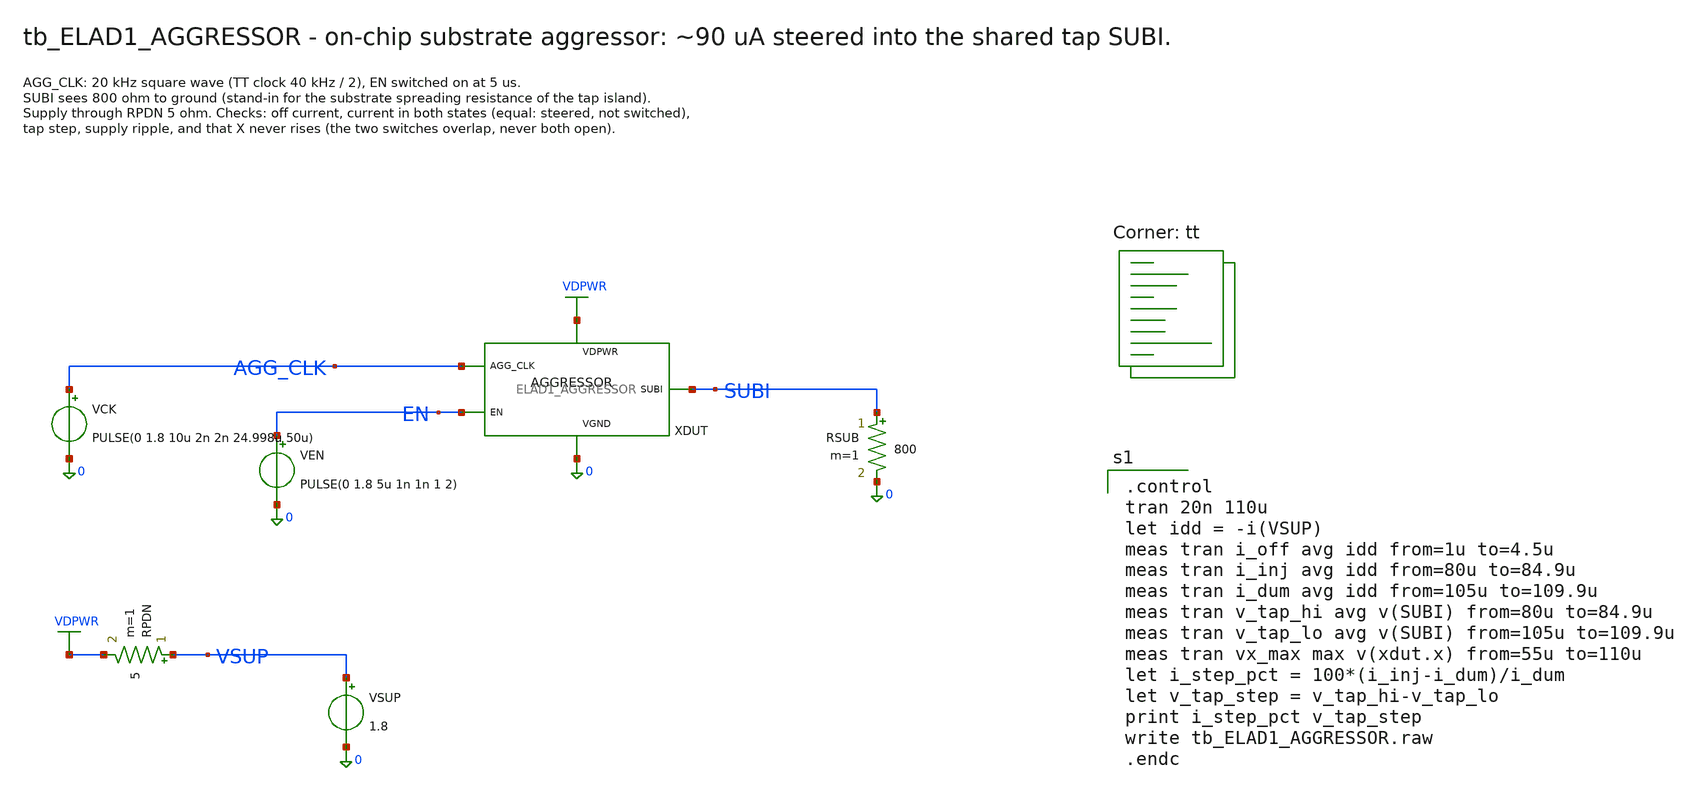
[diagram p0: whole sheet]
** sch_path: cells/ELAD1_AGGRESSOR/schematic/tb_ELAD1_AGGRESSOR.sch
**.subckt tb_ELAD1_AGGRESSOR
XDUT AGG_CLK EN VDPWR 0 SUBI ELAD1_AGGRESSOR
VEN EN 0 PULSE(0 1.8 5u 1n 1n 1 2)
VCK AGG_CLK 0 PULSE(0 1.8 10u 2n 2n 24.998u 50u)
RSUB SUBI 0 800 m=1
RPDN VSUP VDPWR 5 m=1
VSUP VSUP 0 1.8
**** begin user architecture code

.control
tran 20n 110u
let idd = -i(VSUP)
meas tran i_off avg idd from=1u to=4.5u
meas tran i_inj avg idd from=80u to=84.9u
meas tran i_dum avg idd from=105u to=109.9u
meas tran v_tap_hi avg v(SUBI) from=80u to=84.9u
meas tran v_tap_lo avg v(SUBI) from=105u to=109.9u
meas tran vx_max max v(xdut.x) from=55u to=110u
let i_step_pct = 100*(i_inj-i_dum)/i_dum
let v_tap_step = v_tap_hi-v_tap_lo
print i_step_pct v_tap_step
write tb_ELAD1_AGGRESSOR.raw
.endc

.lib $::SKYWATER_MODELS/sky130.lib.spice tt
**** end user architecture code
**.ends

* expanding   symbol:  ELAD1_AGGRESSOR.sym # of pins=5
** sym_path: cells/ELAD1_AGGRESSOR/schematic/ELAD1_AGGRESSOR.sym
** sch_path: cells/ELAD1_AGGRESSOR/schematic/ELAD1_AGGRESSOR.sch
.subckt ELAD1_AGGRESSOR AGG_CLK EN VDPWR VGND SUBI
*.iopin AGG_CLK
*.iopin EN
*.iopin VDPWR
*.iopin VGND
*.iopin SUBI
XIC AGG_CLK CKB VDPWR VGND ELAD1_INV
XIE EN ENB VDPWR VGND ELAD1_INV
XGIP1 gip ENB VDPWR VDPWR sky130_fd_pr__pfet_01v8 L=0.15 W=2 nf=1 ad='int((nf+1)/2) * W/nf * 0.29' as='int((nf+2)/2) * W/nf * 0.29'
+ pd='2*int((nf+1)/2) * (W/nf + 0.29)' ps='2*int((nf+2)/2) * (W/nf + 0.29)' nrd='0.29 / W' nrs='0.29 / W'
+ sa=0 sb=0 sd=0 mult=1 m=1
XGIP2 GI CKB gip VDPWR sky130_fd_pr__pfet_01v8 L=0.15 W=2 nf=1 ad='int((nf+1)/2) * W/nf * 0.29' as='int((nf+2)/2) * W/nf * 0.29'
+ pd='2*int((nf+1)/2) * (W/nf + 0.29)' ps='2*int((nf+2)/2) * (W/nf + 0.29)' nrd='0.29 / W' nrs='0.29 / W'
+ sa=0 sb=0 sd=0 mult=1 m=1
XGIN1 GI ENB VGND VGND sky130_fd_pr__nfet_01v8 L=1 W=0.42 nf=1 ad='int((1 + 1)/2) * 0.42 / 1 * 0.29'
+ as='int((1 + 2)/2) * 0.42 / 1 * 0.29' pd='2*int((1 + 1)/2) * (0.42 / 1 + 0.29)' ps='2*int((1 + 2)/2) * (0.42 / 1 + 0.29)'
+ nrd='0.29 / 0.42 ' nrs='0.29 / 0.42 ' sa=0 sb=0 sd=0 mult=1 m=1
XGIN2 GI CKB VGND VGND sky130_fd_pr__nfet_01v8 L=1 W=0.42 nf=1 ad='int((1 + 1)/2) * 0.42 / 1 * 0.29'
+ as='int((1 + 2)/2) * 0.42 / 1 * 0.29' pd='2*int((1 + 1)/2) * (0.42 / 1 + 0.29)' ps='2*int((1 + 2)/2) * (0.42 / 1 + 0.29)'
+ nrd='0.29 / 0.42 ' nrs='0.29 / 0.42 ' sa=0 sb=0 sd=0 mult=1 m=1
XGDP1 gdp ENB VDPWR VDPWR sky130_fd_pr__pfet_01v8 L=0.15 W=2 nf=1 ad='int((nf+1)/2) * W/nf * 0.29' as='int((nf+2)/2) * W/nf * 0.29'
+ pd='2*int((nf+1)/2) * (W/nf + 0.29)' ps='2*int((nf+2)/2) * (W/nf + 0.29)' nrd='0.29 / W' nrs='0.29 / W'
+ sa=0 sb=0 sd=0 mult=1 m=1
XGDP2 GD AGG_CLK gdp VDPWR sky130_fd_pr__pfet_01v8 L=0.15 W=2 nf=1 ad='int((nf+1)/2) * W/nf * 0.29' as='int((nf+2)/2) * W/nf * 0.29'
+ pd='2*int((nf+1)/2) * (W/nf + 0.29)' ps='2*int((nf+2)/2) * (W/nf + 0.29)' nrd='0.29 / W' nrs='0.29 / W'
+ sa=0 sb=0 sd=0 mult=1 m=1
XGDN1 GD ENB VGND VGND sky130_fd_pr__nfet_01v8 L=1 W=0.42 nf=1 ad='int((1 + 1)/2) * 0.42 / 1 * 0.29'
+ as='int((1 + 2)/2) * 0.42 / 1 * 0.29' pd='2*int((1 + 1)/2) * (0.42 / 1 + 0.29)' ps='2*int((1 + 2)/2) * (0.42 / 1 + 0.29)'
+ nrd='0.29 / 0.42 ' nrs='0.29 / 0.42 ' sa=0 sb=0 sd=0 mult=1 m=1
XGDN2 GD AGG_CLK VGND VGND sky130_fd_pr__nfet_01v8 L=1 W=0.42 nf=1 ad='int((1 + 1)/2) * 0.42 / 1 * 0.29'
+ as='int((1 + 2)/2) * 0.42 / 1 * 0.29' pd='2*int((1 + 1)/2) * (0.42 / 1 + 0.29)' ps='2*int((1 + 2)/2) * (0.42 / 1 + 0.29)'
+ nrd='0.29 / 0.42 ' nrs='0.29 / 0.42 ' sa=0 sb=0 sd=0 mult=1 m=1
XRL X VDPWR VGND sky130_fd_pr__res_xhigh_po W=0.69 L=7.3 mult=1 m=1
XMINJ X GI SUBI VGND sky130_fd_pr__nfet_01v8 L=0.15 W=2 nf=1 ad='int((1 + 1)/2) * 2 / 1 * 0.29' as='int((1 + 2)/2) * 2 / 1 * 0.29'
+ pd='2*int((1 + 1)/2) * (2 / 1 + 0.29)' ps='2*int((1 + 2)/2) * (2 / 1 + 0.29)' nrd='0.29 / 2 ' nrs='0.29 / 2 '
+ sa=0 sb=0 sd=0 mult=1 m=1
XMDUM X GD D VGND sky130_fd_pr__nfet_01v8 L=0.15 W=2 nf=1 ad='int((1 + 1)/2) * 2 / 1 * 0.29' as='int((1 + 2)/2) * 2 / 1 * 0.29'
+ pd='2*int((1 + 1)/2) * (2 / 1 + 0.29)' ps='2*int((1 + 2)/2) * (2 / 1 + 0.29)' nrd='0.29 / 2 ' nrs='0.29 / 2 '
+ sa=0 sb=0 sd=0 mult=1 m=1
XRDUM VGND D sky130_fd_pr__res_generic_po W=1 L=15 m=1
.ends


* expanding   symbol:  ELAD1_INV.sym # of pins=4
** sym_path: cells/ELAD1_INV/schematic/ELAD1_INV.sym
** sch_path: cells/ELAD1_INV/schematic/ELAD1_INV.sch
.subckt ELAD1_INV A Y VDPWR VGND
*.iopin A
*.iopin Y
*.iopin VDPWR
*.iopin VGND
XMN Y A VGND VGND sky130_fd_pr__nfet_01v8 L=0.15 W=0.65 nf=1 ad='int((1 + 1)/2) * 0.65 / 1 * 0.29' as='int((1 + 2)/2) * 0.65 / 1 * 0.29'
+ pd='2*int((1 + 1)/2) * (0.65 / 1 + 0.29)' ps='2*int((1 + 2)/2) * (0.65 / 1 + 0.29)' nrd='0.29 / 0.65 '
+ nrs='0.29 / 0.65 ' sa=0 sb=0 sd=0 mult=1 m=1
XMP Y A VDPWR VDPWR sky130_fd_pr__pfet_01v8 L=0.15 W=1 nf=1 ad='int((nf+1)/2) * W/nf * 0.29' as='int((nf+2)/2) * W/nf * 0.29'
+ pd='2*int((nf+1)/2) * (W/nf + 0.29)' ps='2*int((nf+2)/2) * (W/nf + 0.29)' nrd='0.29 / W' nrs='0.29 / W'
+ sa=0 sb=0 sd=0 mult=1 m=1
.ends

.GLOBAL VGND
.GLOBAL VDPWR
.end
